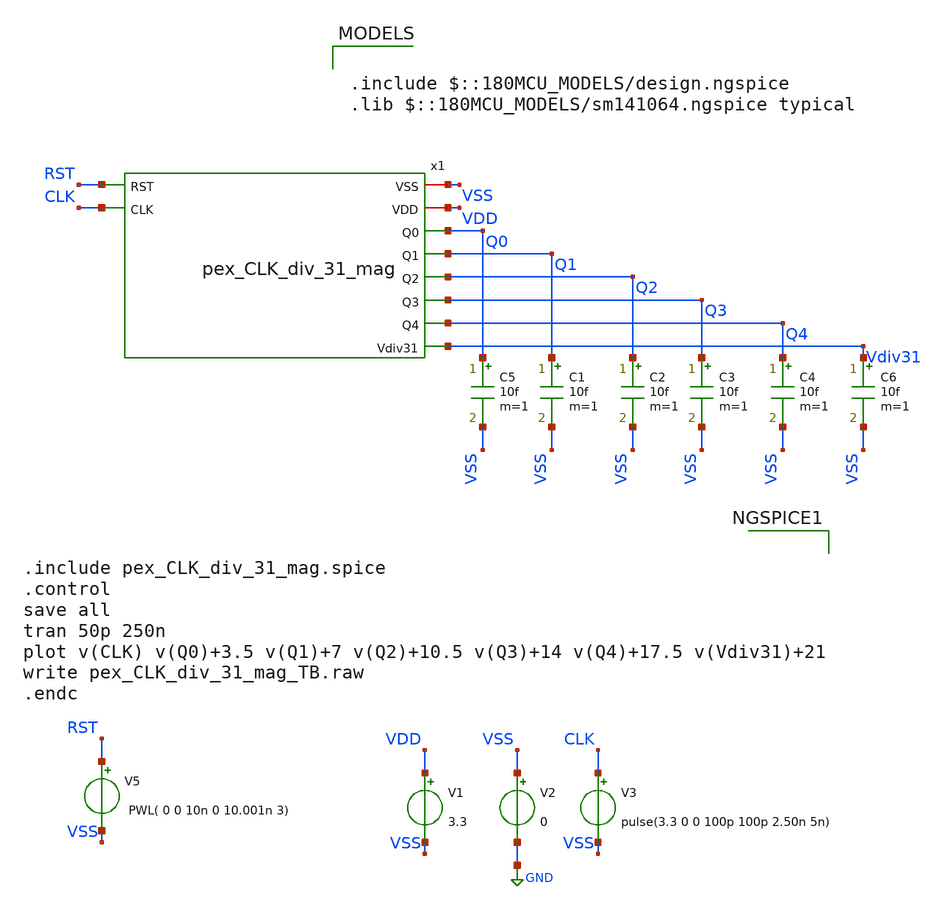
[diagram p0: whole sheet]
** sch_path: Clock_Generator_PAKISTAN_02/xschem/pex_CLK_div_31_mag_TB.sch
**.subckt pex_CLK_div_31_mag_TB
V1 VDD VSS 3.3
V2 VSS GND 0
V3 CLK VSS pulse(3.3 0 0 100p 100p 2.50n 5n)
C5 Q0 VSS 10f m=1
C1 Q1 VSS 10f m=1
C2 Q2 VSS 10f m=1
C3 Q3 VSS 10f m=1
C4 Q4 VSS 10f m=1
C6 Vdiv31 VSS 10f m=1
V5 RST VSS PWL( 0 0 10n 0 10.001n 3)
x1 VSS VDD Q0 Q1 Q2 Q3 Q4 Vdiv31 RST CLK pex_CLK_div_31_mag
**** begin user architecture code

.include $::180MCU_MODELS/design.ngspice
.lib $::180MCU_MODELS/sm141064.ngspice typical



.include pex_CLK_div_31_mag.spice
.control
save all
tran 50p 250n
plot v(CLK) v(Q0)+3.5 v(Q1)+7 v(Q2)+10.5 v(Q3)+14 v(Q4)+17.5 v(Vdiv31)+21
write pex_CLK_div_31_mag_TB.raw
.endc


**** end user architecture code
**.ends
.GLOBAL GND
.end
